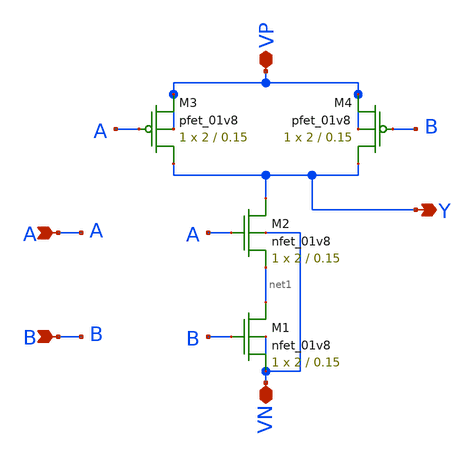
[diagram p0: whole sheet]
** sch_path: mp1/submission/Xschem/nand.sch
**.subckt nand A B VP VN Y
*.ipin A
*.ipin B
*.iopin VP
*.iopin VN
*.opin Y
XM1 net1 B VN VN sky130_fd_pr__nfet_01v8 L=0.15 W=2 nf=1 ad='int((nf+1)/2) * W/nf * 0.29' as='int((nf+2)/2) * W/nf * 0.29'
+ pd='2*int((nf+1)/2) * (W/nf + 0.29)' ps='2*int((nf+2)/2) * (W/nf + 0.29)' nrd='0.29 / W' nrs='0.29 / W'
+ sa=0 sb=0 sd=0 mult=1 m=1
XM2 Y A net1 VN sky130_fd_pr__nfet_01v8 L=0.15 W=2 nf=1 ad='int((nf+1)/2) * W/nf * 0.29' as='int((nf+2)/2) * W/nf * 0.29'
+ pd='2*int((nf+1)/2) * (W/nf + 0.29)' ps='2*int((nf+2)/2) * (W/nf + 0.29)' nrd='0.29 / W' nrs='0.29 / W'
+ sa=0 sb=0 sd=0 mult=1 m=1
XM3 Y A VP VP sky130_fd_pr__pfet_01v8 L=0.15 W=2 nf=1 ad='int((nf+1)/2) * W/nf * 0.29' as='int((nf+2)/2) * W/nf * 0.29'
+ pd='2*int((nf+1)/2) * (W/nf + 0.29)' ps='2*int((nf+2)/2) * (W/nf + 0.29)' nrd='0.29 / W' nrs='0.29 / W'
+ sa=0 sb=0 sd=0 mult=1 m=1
XM4 Y B VP VP sky130_fd_pr__pfet_01v8 L=0.15 W=2 nf=1 ad='int((nf+1)/2) * W/nf * 0.29' as='int((nf+2)/2) * W/nf * 0.29'
+ pd='2*int((nf+1)/2) * (W/nf + 0.29)' ps='2*int((nf+2)/2) * (W/nf + 0.29)' nrd='0.29 / W' nrs='0.29 / W'
+ sa=0 sb=0 sd=0 mult=1 m=1
**.ends
.end
